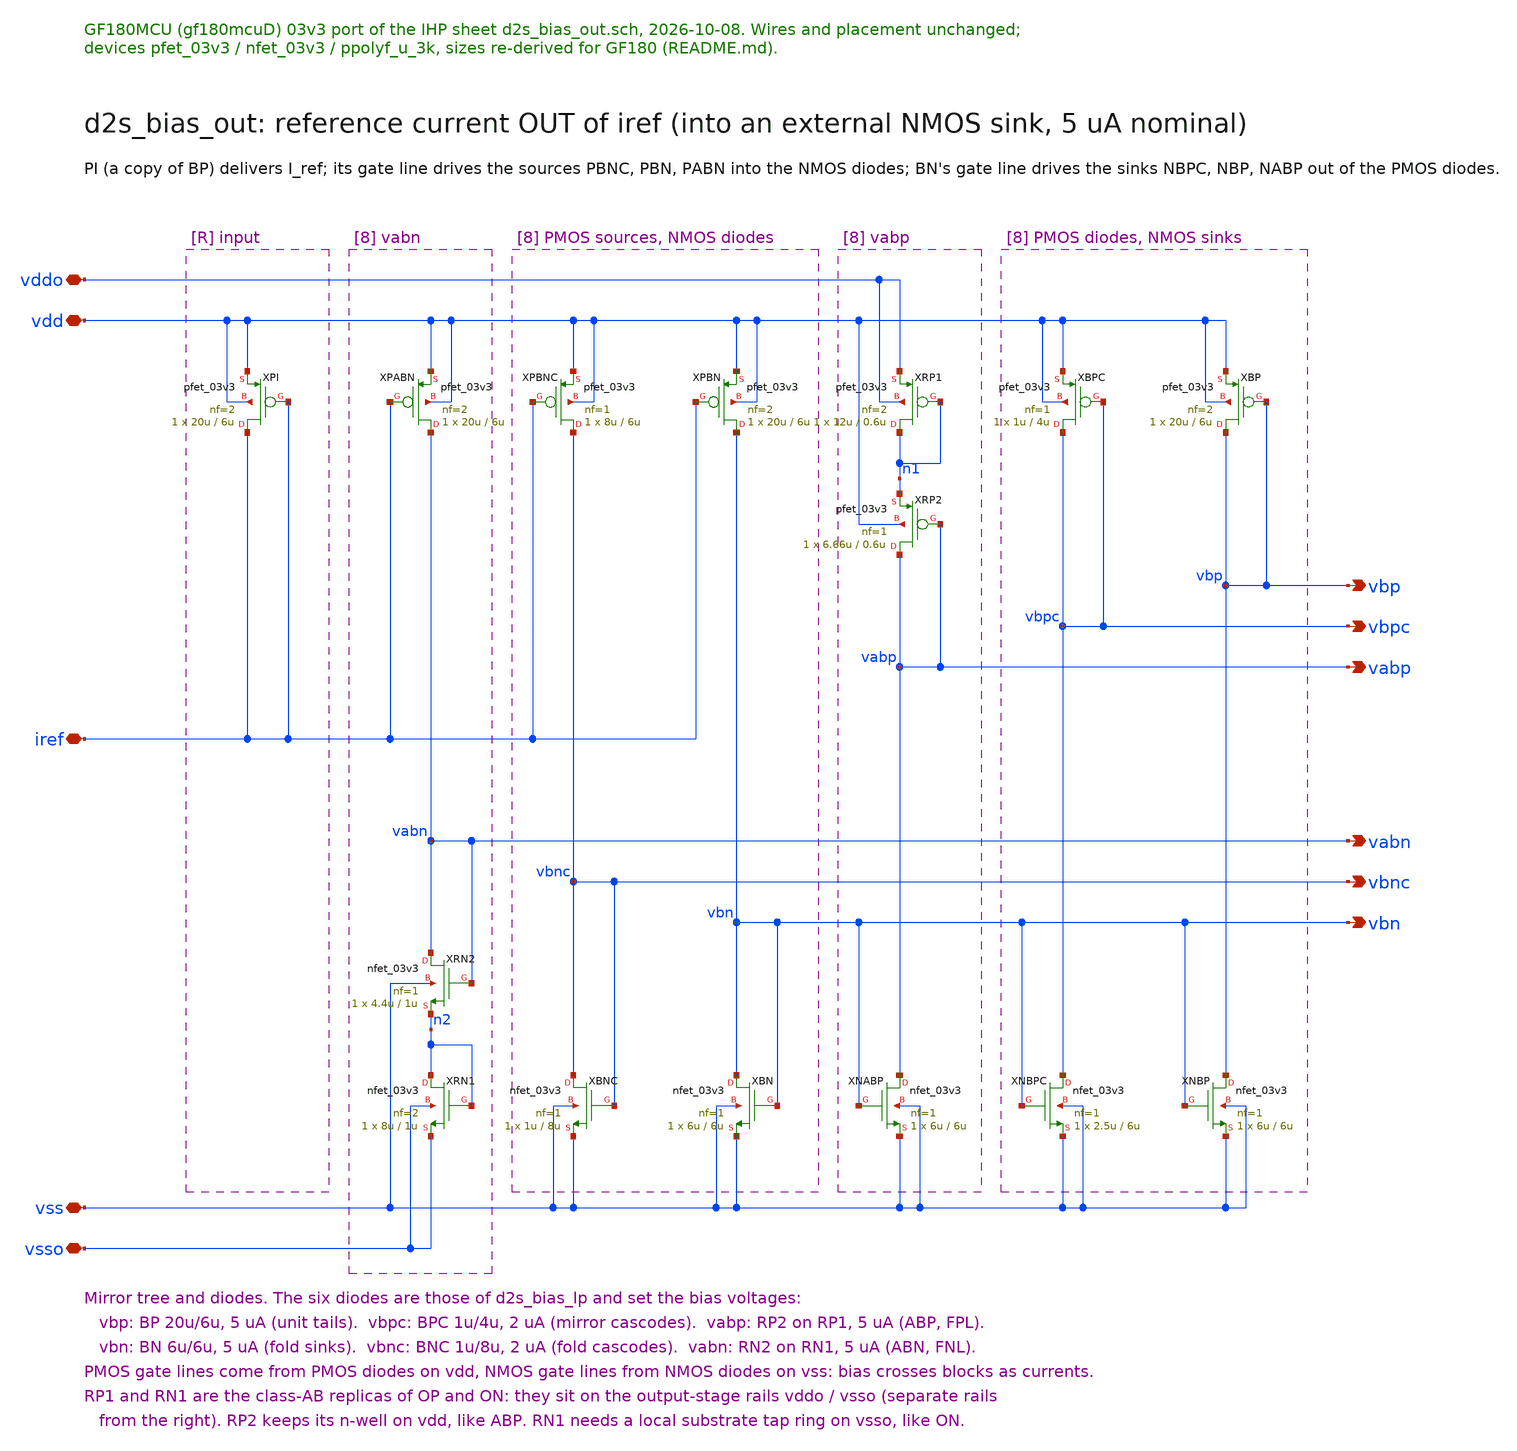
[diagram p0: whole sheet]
** sch_path: macros/ClassABBias/schematic/xschem/ClassABBiasOut.sch
**.subckt ClassABBiasOut vdd vss vddo vsso iref vbp vbn vbpc vbnc vabp vabn
*.iopin vdd
*.iopin vss
*.iopin vddo
*.iopin vsso
*.iopin iref
*.opin vbp
*.opin vbn
*.opin vbpc
*.opin vbnc
*.opin vabp
*.opin vabn
XPI iref iref vdd vdd pfet_03v3 L=6u W=20u nf=2 ad='int((nf+1)/2) * W/nf * 0.18u' as='int((nf+2)/2) * W/nf * 0.18u'
+ pd='2*int((nf+1)/2) * (W/nf + 0.18u)' ps='2*int((nf+2)/2) * (W/nf + 0.18u)' nrd='0.18u / W' nrs='0.18u / W'
+ sa=0 sb=0 sd=0 m=1
XBPC vbpc vbpc vdd vdd pfet_03v3 L=4u W=1u nf=1 ad='int((nf+1)/2) * W/nf * 0.18u' as='int((nf+2)/2) * W/nf * 0.18u'
+ pd='2*int((nf+1)/2) * (W/nf + 0.18u)' ps='2*int((nf+2)/2) * (W/nf + 0.18u)' nrd='0.18u / W' nrs='0.18u / W'
+ sa=0 sb=0 sd=0 m=1
XNBPC vbpc vbn vss vss nfet_03v3 L=6u W=2.5u nf=1 ad='int((nf+1)/2) * W/nf * 0.18u' as='int((nf+2)/2) * W/nf * 0.18u'
+ pd='2*int((nf+1)/2) * (W/nf + 0.18u)' ps='2*int((nf+2)/2) * (W/nf + 0.18u)' nrd='0.18u / W' nrs='0.18u / W'
+ sa=0 sb=0 sd=0 m=1
XBP vbp vbp vdd vdd pfet_03v3 L=6u W=20u nf=2 ad='int((nf+1)/2) * W/nf * 0.18u' as='int((nf+2)/2) * W/nf * 0.18u'
+ pd='2*int((nf+1)/2) * (W/nf + 0.18u)' ps='2*int((nf+2)/2) * (W/nf + 0.18u)' nrd='0.18u / W' nrs='0.18u / W'
+ sa=0 sb=0 sd=0 m=1
XNBP vbp vbn vss vss nfet_03v3 L=6u W=6u nf=1 ad='int((nf+1)/2) * W/nf * 0.18u' as='int((nf+2)/2) * W/nf * 0.18u'
+ pd='2*int((nf+1)/2) * (W/nf + 0.18u)' ps='2*int((nf+2)/2) * (W/nf + 0.18u)' nrd='0.18u / W' nrs='0.18u / W'
+ sa=0 sb=0 sd=0 m=1
XRP1 n1 n1 vddo vddo pfet_03v3 L=0.6u W=12u nf=2 ad='int((nf+1)/2) * W/nf * 0.18u' as='int((nf+2)/2) * W/nf * 0.18u'
+ pd='2*int((nf+1)/2) * (W/nf + 0.18u)' ps='2*int((nf+2)/2) * (W/nf + 0.18u)' nrd='0.18u / W' nrs='0.18u / W'
+ sa=0 sb=0 sd=0 m=1
XRP2 vabp vabp n1 vdd pfet_03v3 L=0.6u W=6.66u nf=1 ad='int((nf+1)/2) * W/nf * 0.18u' as='int((nf+2)/2) * W/nf * 0.18u'
+ pd='2*int((nf+1)/2) * (W/nf + 0.18u)' ps='2*int((nf+2)/2) * (W/nf + 0.18u)' nrd='0.18u / W' nrs='0.18u / W'
+ sa=0 sb=0 sd=0 m=1
XNABP vabp vbn vss vss nfet_03v3 L=6u W=6u nf=1 ad='int((nf+1)/2) * W/nf * 0.18u' as='int((nf+2)/2) * W/nf * 0.18u'
+ pd='2*int((nf+1)/2) * (W/nf + 0.18u)' ps='2*int((nf+2)/2) * (W/nf + 0.18u)' nrd='0.18u / W' nrs='0.18u / W'
+ sa=0 sb=0 sd=0 m=1
XPBNC vbnc iref vdd vdd pfet_03v3 L=6u W=8u nf=1 ad='int((nf+1)/2) * W/nf * 0.18u' as='int((nf+2)/2) * W/nf * 0.18u'
+ pd='2*int((nf+1)/2) * (W/nf + 0.18u)' ps='2*int((nf+2)/2) * (W/nf + 0.18u)' nrd='0.18u / W' nrs='0.18u / W'
+ sa=0 sb=0 sd=0 m=1
XBNC vbnc vbnc vss vss nfet_03v3 L=8u W=1u nf=1 ad='int((nf+1)/2) * W/nf * 0.18u' as='int((nf+2)/2) * W/nf * 0.18u'
+ pd='2*int((nf+1)/2) * (W/nf + 0.18u)' ps='2*int((nf+2)/2) * (W/nf + 0.18u)' nrd='0.18u / W' nrs='0.18u / W'
+ sa=0 sb=0 sd=0 m=1
XPBN vbn iref vdd vdd pfet_03v3 L=6u W=20u nf=2 ad='int((nf+1)/2) * W/nf * 0.18u' as='int((nf+2)/2) * W/nf * 0.18u'
+ pd='2*int((nf+1)/2) * (W/nf + 0.18u)' ps='2*int((nf+2)/2) * (W/nf + 0.18u)' nrd='0.18u / W' nrs='0.18u / W'
+ sa=0 sb=0 sd=0 m=1
XBN vbn vbn vss vss nfet_03v3 L=6u W=6u nf=1 ad='int((nf+1)/2) * W/nf * 0.18u' as='int((nf+2)/2) * W/nf * 0.18u'
+ pd='2*int((nf+1)/2) * (W/nf + 0.18u)' ps='2*int((nf+2)/2) * (W/nf + 0.18u)' nrd='0.18u / W' nrs='0.18u / W'
+ sa=0 sb=0 sd=0 m=1
XPABN vabn iref vdd vdd pfet_03v3 L=6u W=20u nf=2 ad='int((nf+1)/2) * W/nf * 0.18u' as='int((nf+2)/2) * W/nf * 0.18u'
+ pd='2*int((nf+1)/2) * (W/nf + 0.18u)' ps='2*int((nf+2)/2) * (W/nf + 0.18u)' nrd='0.18u / W' nrs='0.18u / W'
+ sa=0 sb=0 sd=0 m=1
XRN2 vabn vabn n2 vss nfet_03v3 L=1u W=4.4u nf=1 ad='int((nf+1)/2) * W/nf * 0.18u' as='int((nf+2)/2) * W/nf * 0.18u'
+ pd='2*int((nf+1)/2) * (W/nf + 0.18u)' ps='2*int((nf+2)/2) * (W/nf + 0.18u)' nrd='0.18u / W' nrs='0.18u / W'
+ sa=0 sb=0 sd=0 m=1
XRN1 n2 n2 vsso vsso nfet_03v3 L=1u W=8u nf=2 ad='int((nf+1)/2) * W/nf * 0.18u' as='int((nf+2)/2) * W/nf * 0.18u'
+ pd='2*int((nf+1)/2) * (W/nf + 0.18u)' ps='2*int((nf+2)/2) * (W/nf + 0.18u)' nrd='0.18u / W' nrs='0.18u / W'
+ sa=0 sb=0 sd=0 m=1
**.ends
.end
